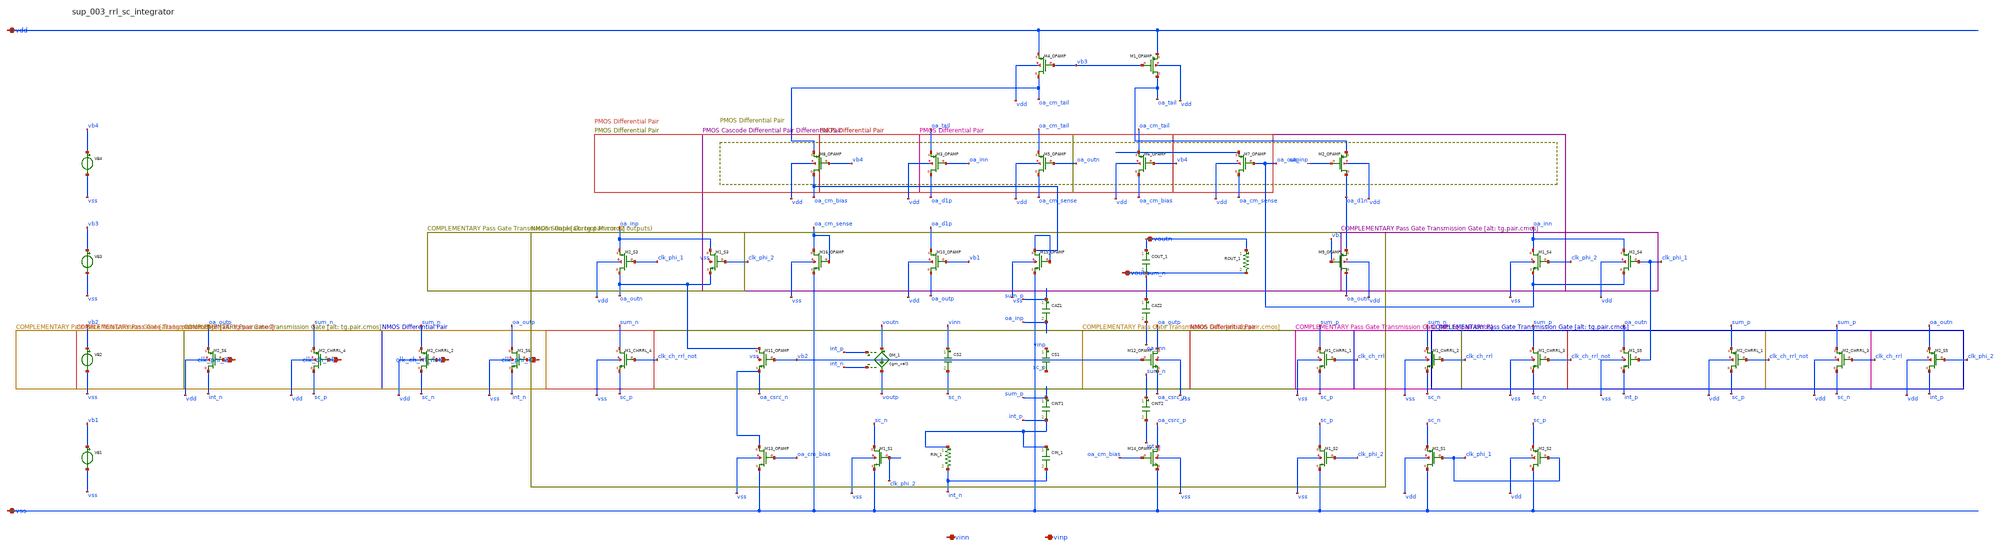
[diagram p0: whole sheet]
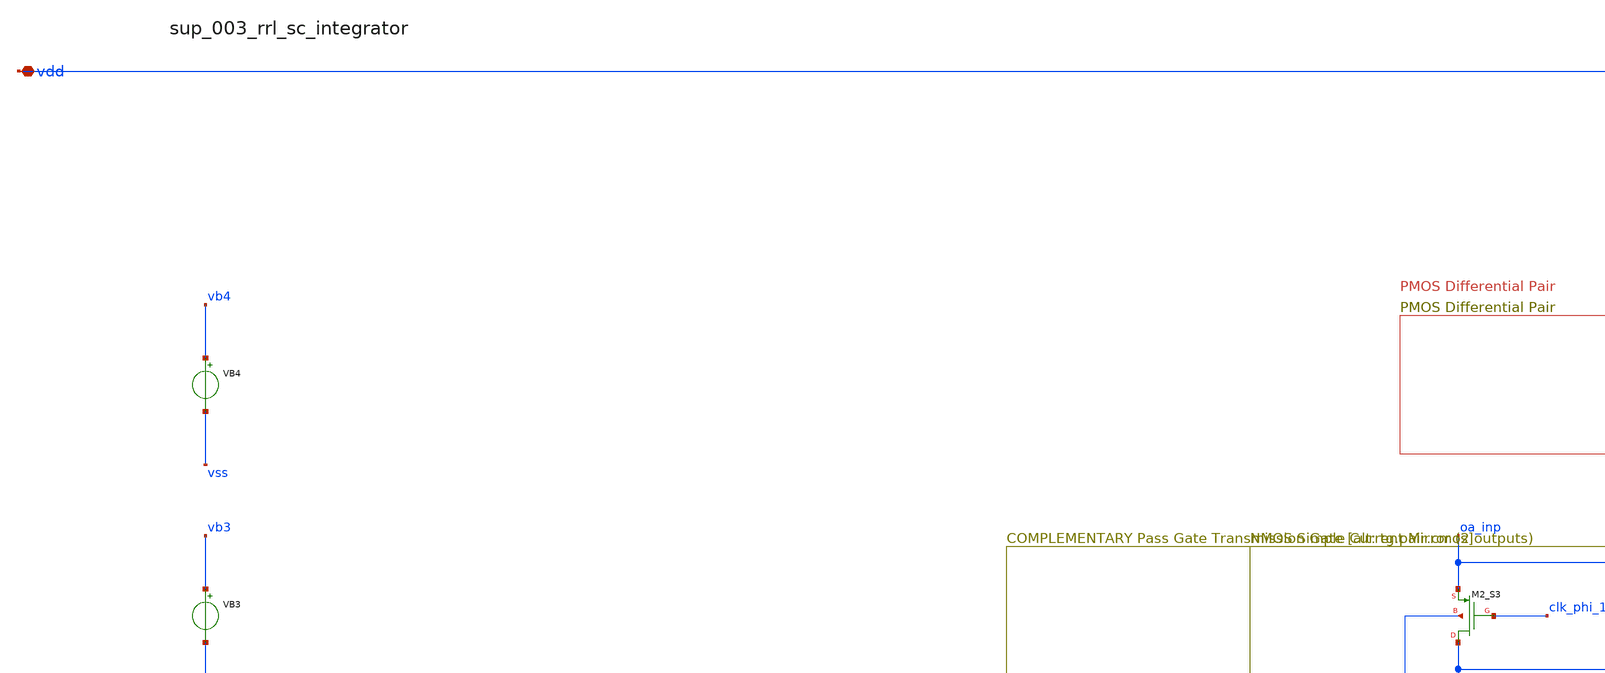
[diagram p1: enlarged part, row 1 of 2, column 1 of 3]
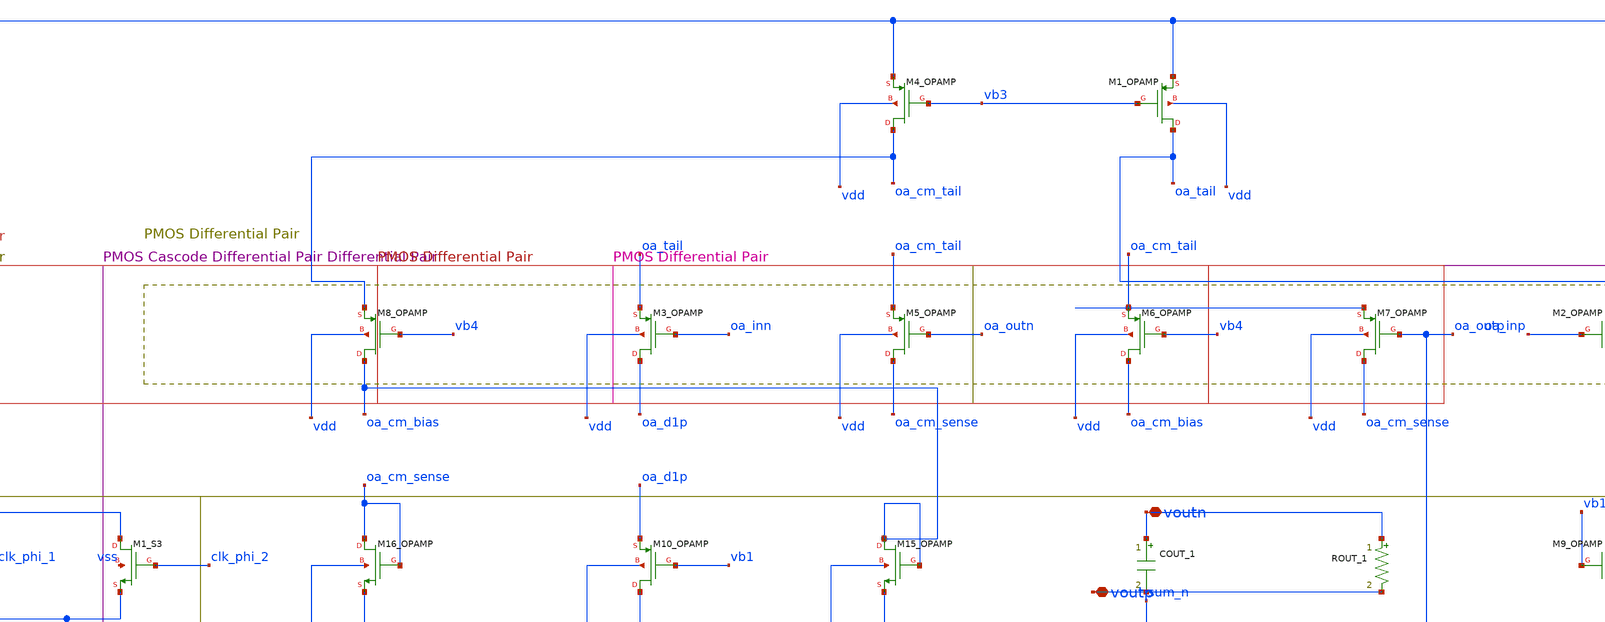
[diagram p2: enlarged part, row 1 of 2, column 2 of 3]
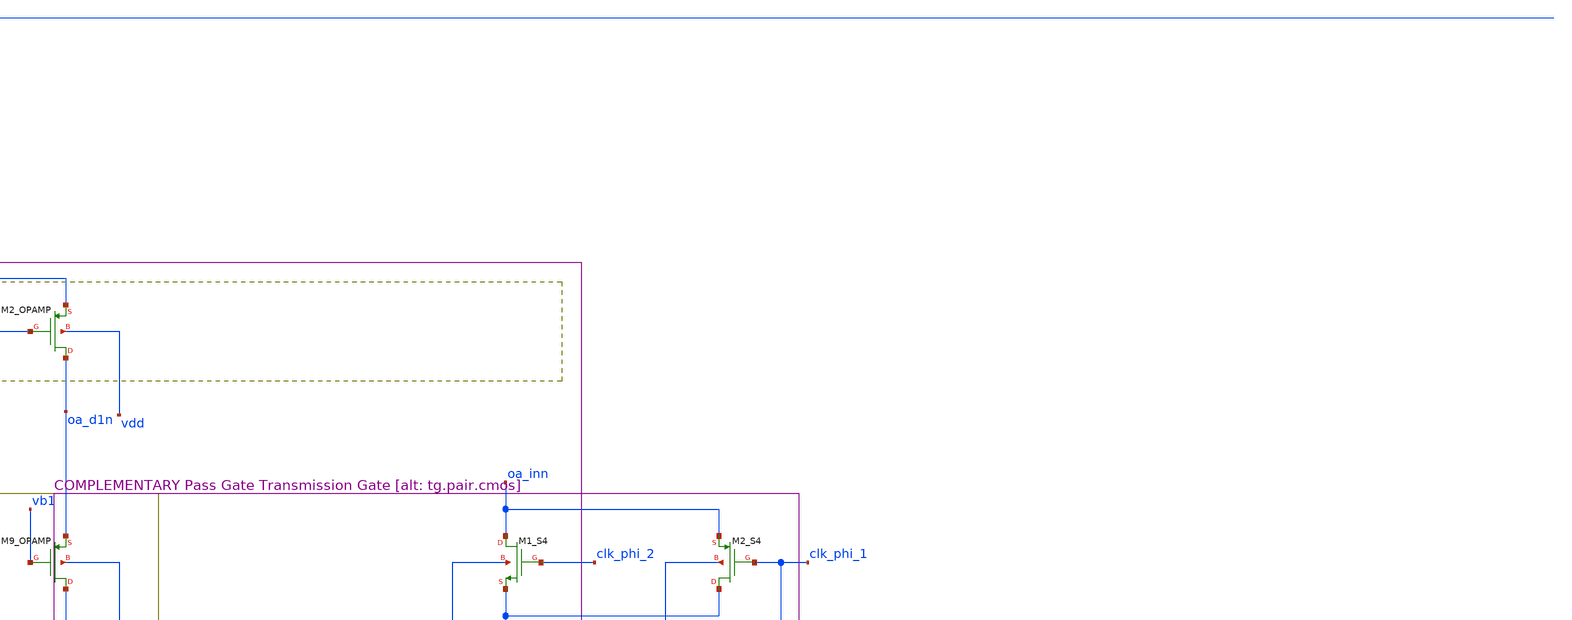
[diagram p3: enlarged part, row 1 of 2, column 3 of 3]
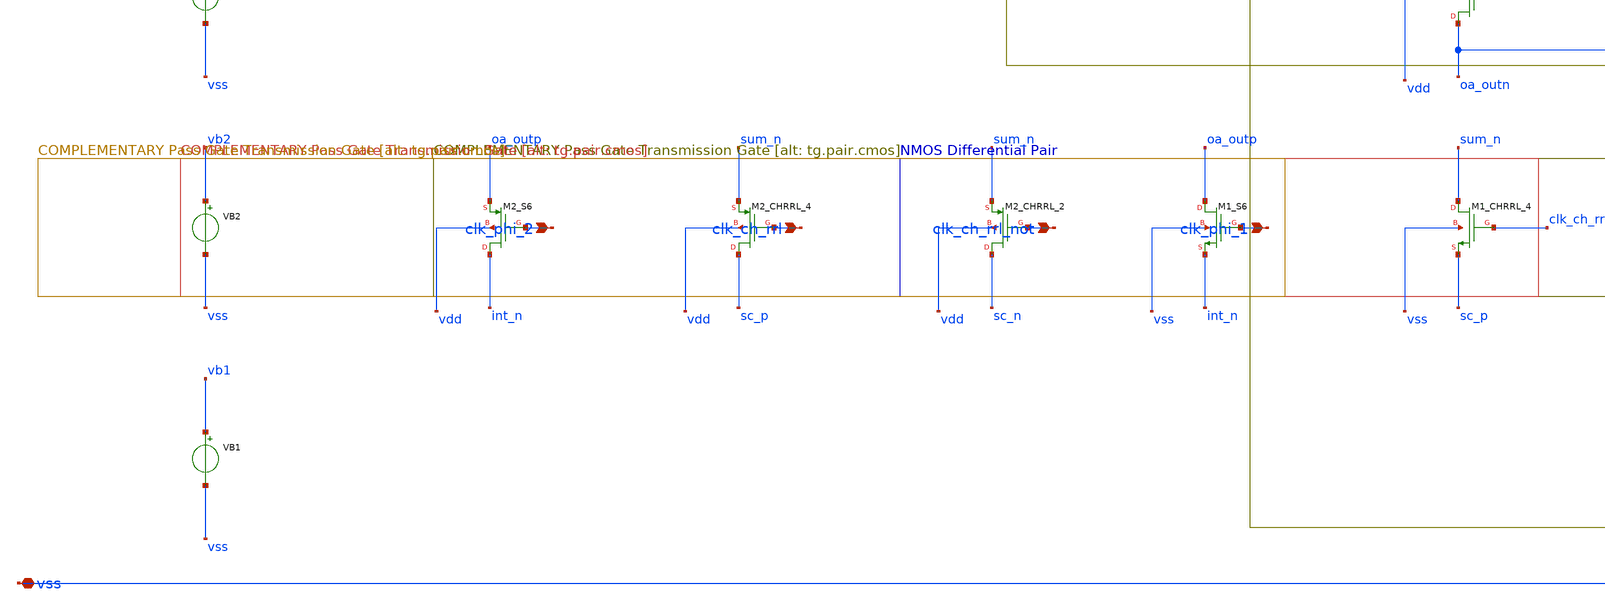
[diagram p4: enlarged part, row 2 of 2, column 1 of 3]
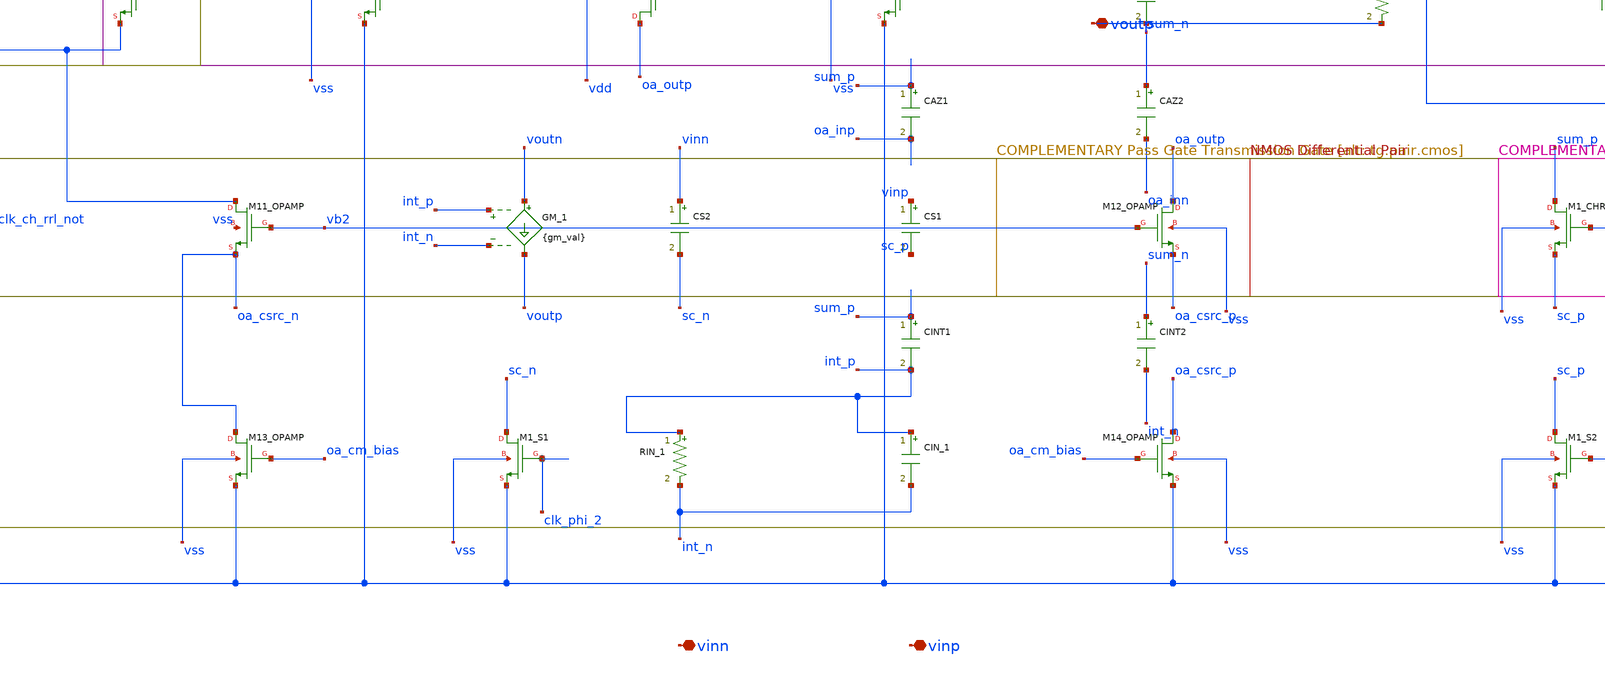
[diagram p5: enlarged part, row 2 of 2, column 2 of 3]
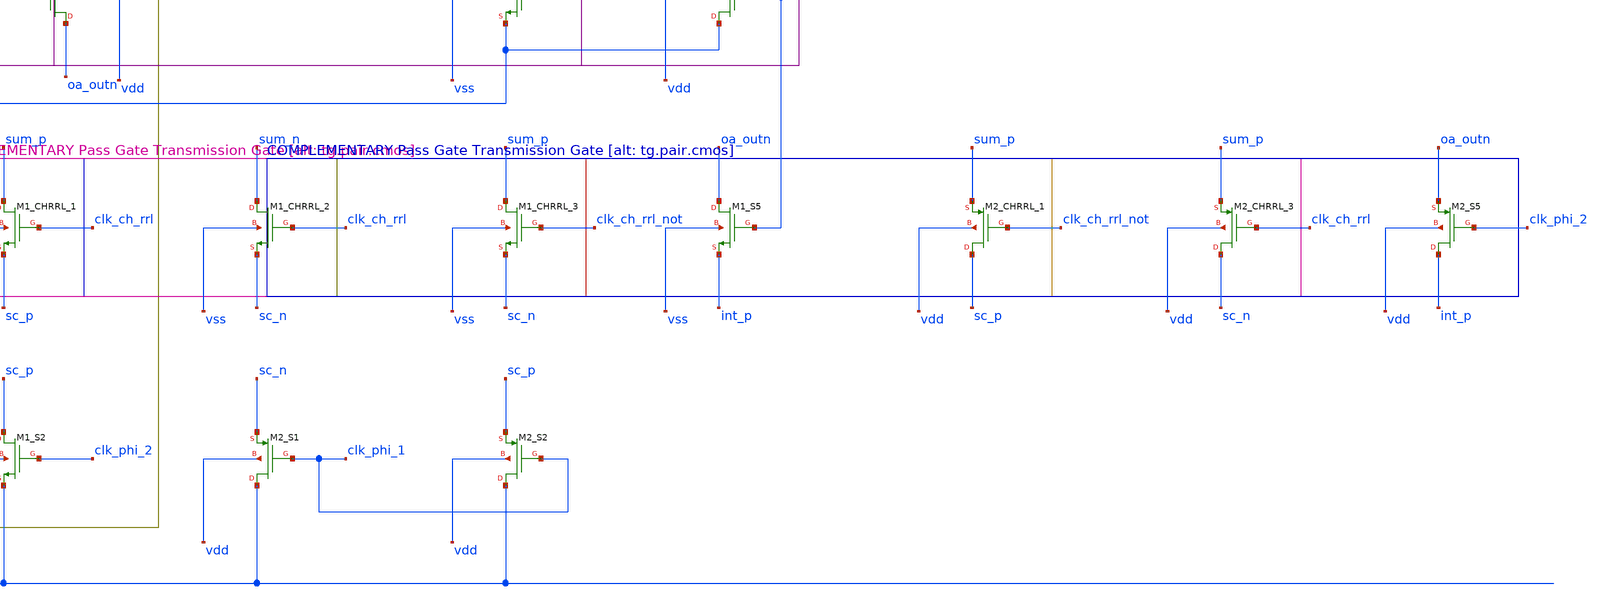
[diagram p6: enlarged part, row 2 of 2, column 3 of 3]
** sch_path: analog-db/raw/sup_003_rrl_sc_integrator/sup_003_rrl_sc_integrator_annotated.sch
**.subckt sup_003_rrl_sc_integrator_annotated clk_phi_1 clk_phi_2 clk_ch_rrl clk_ch_rrl_not vdd vss
*+ voutn voutp vinn vinp
*.ipin clk_phi_1
*.ipin clk_phi_2
*.ipin clk_ch_rrl
*.ipin clk_ch_rrl_not
*.iopin vdd
*.iopin vss
*.iopin voutn
*.iopin voutp
*.iopin vinn
*.iopin vinp
CAZ1 sum_p oa_inp 'x_dut_caz1_value' m=1
CAZ2 sum_n oa_inn 'x_dut_caz2_value' m=1
CINT1 sum_p int_p 'x_dut_cint1_value' m=1
CINT2 sum_n int_n 'x_dut_cint2_value' m=1
CIN_1 int_p int_n 'cin_val' m=1
COUT_1 voutn voutp 'cout_val' m=1
CS1 vinp sc_p 'x_dut_cs1_value' m=1
CS2 vinn sc_n 'x_dut_cs2_value' m=1
GM_1 voutn voutp int_p int_n {gm_val}
RIN_1 int_p int_n 'rin_val' m=1
ROUT_1 voutn voutp 'rout_val' m=1
VB1 vb1 vss dc {vb1}
VB2 vb2 vss dc {vb2}
VB3 vb3 vss dc {vb3}
VB4 vb4 vss dc {vb4}
XM10_OPAMP oa_outp vb1 oa_d1p vdd sg13_lv_pmos w=x_dut_xm10_opamp_w l=x_dut_xm10_opamp_l ng=1
+ m=x_dut_xm10_opamp_m
XM11_OPAMP oa_outn vb2 oa_csrc_n vss sg13_lv_nmos w=x_dut_xm11_opamp_w l=x_dut_xm11_opamp_l ng=1
+ m=x_dut_xm11_opamp_m
XM12_OPAMP oa_outp vb2 oa_csrc_p vss sg13_lv_nmos w=x_dut_xm12_opamp_w l=x_dut_xm12_opamp_l ng=1
+ m=x_dut_xm12_opamp_m
XM13_OPAMP oa_csrc_n oa_cm_bias vss vss sg13_lv_nmos w=x_dut_xm13_opamp_w l=x_dut_xm13_opamp_l ng=1
+ m=x_dut_xm13_opamp_m
XM14_OPAMP oa_csrc_p oa_cm_bias vss vss sg13_lv_nmos w=x_dut_xm14_opamp_w l=x_dut_xm14_opamp_l ng=1
+ m=x_dut_xm14_opamp_m
XM15_OPAMP oa_cm_bias oa_cm_bias vss vss sg13_lv_nmos w=x_dut_xm15_opamp_w l=x_dut_xm15_opamp_l ng=1
+ m=x_dut_xm15_opamp_m
XM16_OPAMP oa_cm_sense oa_cm_sense vss vss sg13_lv_nmos w=x_dut_xm16_opamp_w l=x_dut_xm16_opamp_l
+ ng=1 m=x_dut_xm16_opamp_m
XM1_CHRRL_1 sum_p clk_ch_rrl sc_p vss sg13_lv_nmos w=x_dut_xm1_chrrl_1_w l=x_dut_xm1_chrrl_1_l ng=1
+ m=x_dut_xm1_chrrl_1_m
XM1_CHRRL_2 sum_n clk_ch_rrl sc_n vss sg13_lv_nmos w=x_dut_xm1_chrrl_2_w l=x_dut_xm1_chrrl_2_l ng=1
+ m=x_dut_xm1_chrrl_2_m
XM1_CHRRL_3 sum_p clk_ch_rrl_not sc_n vss sg13_lv_nmos w=x_dut_xm1_chrrl_3_w l=x_dut_xm1_chrrl_3_l
+ ng=1 m=x_dut_xm1_chrrl_3_m
XM1_CHRRL_4 sum_n clk_ch_rrl_not sc_p vss sg13_lv_nmos w=x_dut_xm1_chrrl_4_w l=x_dut_xm1_chrrl_4_l
+ ng=1 m=x_dut_xm1_chrrl_4_m
XM1_OPAMP oa_tail vb3 vdd vdd sg13_lv_pmos w=x_dut_xm1_opamp_w l=x_dut_xm1_opamp_l ng=1
+ m=x_dut_xm1_opamp_m
XM1_S1 sc_n clk_phi_2 vss vss sg13_lv_nmos w=x_dut_xm1_s1_w l=x_dut_xm1_s1_l ng=1 m=x_dut_xm1_s1_m
XM1_S2 sc_p clk_phi_2 vss vss sg13_lv_nmos w=x_dut_xm1_s2_w l=x_dut_xm1_s2_l ng=1 m=x_dut_xm1_s2_m
XM1_S3 oa_inp clk_phi_2 oa_outn vss sg13_lv_nmos w=x_dut_xm1_s3_w l=x_dut_xm1_s3_l ng=1
+ m=x_dut_xm1_s3_m
XM1_S4 oa_inn clk_phi_2 oa_outp vss sg13_lv_nmos w=x_dut_xm1_s4_w l=x_dut_xm1_s4_l ng=1
+ m=x_dut_xm1_s4_m
XM1_S5 oa_outn clk_phi_1 int_p vss sg13_lv_nmos w=x_dut_xm1_s5_w l=x_dut_xm1_s5_l ng=1
+ m=x_dut_xm1_s5_m
XM1_S6 oa_outp clk_phi_1 int_n vss sg13_lv_nmos w=x_dut_xm1_s6_w l=x_dut_xm1_s6_l ng=1
+ m=x_dut_xm1_s6_m
XM2_CHRRL_1 sc_p clk_ch_rrl_not sum_p vdd sg13_lv_pmos w=x_dut_xm2_chrrl_1_w l=x_dut_xm2_chrrl_1_l
+ ng=1 m=x_dut_xm2_chrrl_1_m
XM2_CHRRL_2 sc_n clk_ch_rrl_not sum_n vdd sg13_lv_pmos w=x_dut_xm2_chrrl_2_w l=x_dut_xm2_chrrl_2_l
+ ng=1 m=x_dut_xm2_chrrl_2_m
XM2_CHRRL_3 sc_n clk_ch_rrl sum_p vdd sg13_lv_pmos w=x_dut_xm2_chrrl_3_w l=x_dut_xm2_chrrl_3_l ng=1
+ m=x_dut_xm2_chrrl_3_m
XM2_CHRRL_4 sc_p clk_ch_rrl sum_n vdd sg13_lv_pmos w=x_dut_xm2_chrrl_4_w l=x_dut_xm2_chrrl_4_l ng=1
+ m=x_dut_xm2_chrrl_4_m
XM2_OPAMP oa_d1n oa_inp oa_tail vdd sg13_lv_pmos w=x_dut_xm2_opamp_w l=x_dut_xm2_opamp_l ng=1
+ m=x_dut_xm2_opamp_m
XM2_S1 vss clk_phi_1 sc_n vdd sg13_lv_pmos w=x_dut_xm2_s1_w l=x_dut_xm2_s1_l ng=1 m=x_dut_xm2_s1_m
XM2_S2 vss clk_phi_1 sc_p vdd sg13_lv_pmos w=x_dut_xm2_s2_w l=x_dut_xm2_s2_l ng=1 m=x_dut_xm2_s2_m
XM2_S3 oa_outn clk_phi_1 oa_inp vdd sg13_lv_pmos w=x_dut_xm2_s3_w l=x_dut_xm2_s3_l ng=1
+ m=x_dut_xm2_s3_m
XM2_S4 oa_outp clk_phi_1 oa_inn vdd sg13_lv_pmos w=x_dut_xm2_s4_w l=x_dut_xm2_s4_l ng=1
+ m=x_dut_xm2_s4_m
XM2_S5 int_p clk_phi_2 oa_outn vdd sg13_lv_pmos w=x_dut_xm2_s5_w l=x_dut_xm2_s5_l ng=1
+ m=x_dut_xm2_s5_m
XM2_S6 int_n clk_phi_2 oa_outp vdd sg13_lv_pmos w=x_dut_xm2_s6_w l=x_dut_xm2_s6_l ng=1
+ m=x_dut_xm2_s6_m
XM3_OPAMP oa_d1p oa_inn oa_tail vdd sg13_lv_pmos w=x_dut_xm3_opamp_w l=x_dut_xm3_opamp_l ng=1
+ m=x_dut_xm3_opamp_m
XM4_OPAMP oa_cm_tail vb3 vdd vdd sg13_lv_pmos w=x_dut_xm4_opamp_w l=x_dut_xm4_opamp_l ng=1
+ m=x_dut_xm4_opamp_m
XM5_OPAMP oa_cm_sense oa_outn oa_cm_tail vdd sg13_lv_pmos w=x_dut_xm5_opamp_w l=x_dut_xm5_opamp_l
+ ng=1 m=x_dut_xm5_opamp_m
XM6_OPAMP oa_cm_bias vb4 oa_cm_tail vdd sg13_lv_pmos w=x_dut_xm6_opamp_w l=x_dut_xm6_opamp_l ng=1
+ m=x_dut_xm6_opamp_m
XM7_OPAMP oa_cm_sense oa_outp oa_cm_tail vdd sg13_lv_pmos w=x_dut_xm7_opamp_w l=x_dut_xm7_opamp_l
+ ng=1 m=x_dut_xm7_opamp_m
XM8_OPAMP oa_cm_bias vb4 oa_cm_tail vdd sg13_lv_pmos w=x_dut_xm8_opamp_w l=x_dut_xm8_opamp_l ng=1
+ m=x_dut_xm8_opamp_m
XM9_OPAMP oa_outn vb1 oa_d1n vdd sg13_lv_pmos w=x_dut_xm9_opamp_w l=x_dut_xm9_opamp_l ng=1
+ m=x_dut_xm9_opamp_m
**.ends
.end
